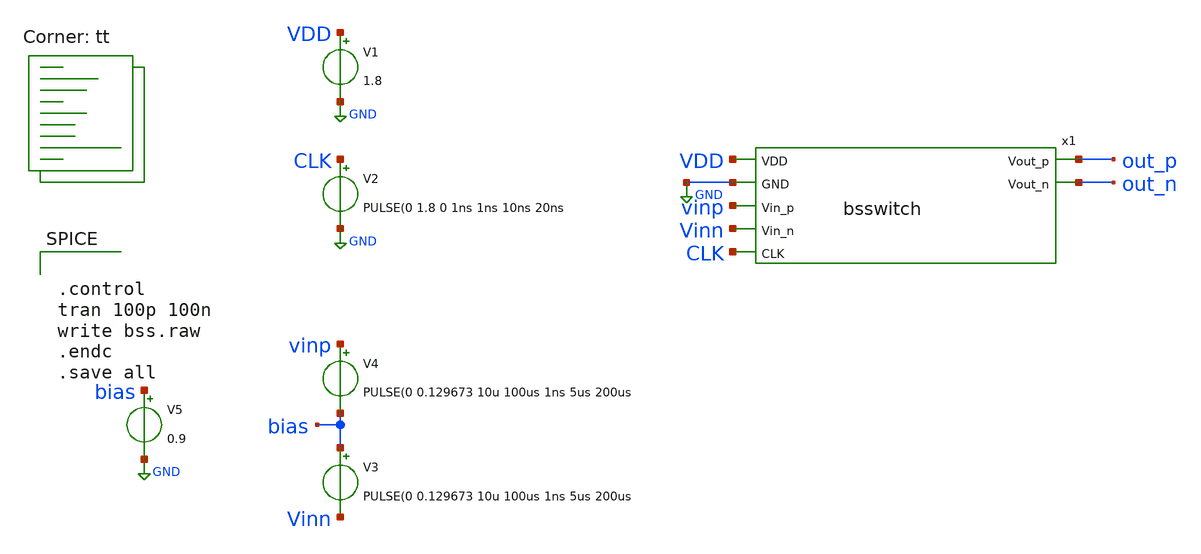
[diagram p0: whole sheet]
** sch_path: xschem/bsswitch_test.sch
**.subckt bsswitch_test
V2 CLK GND PULSE(0 1.8 0 1ns 1ns 10ns 20ns
V1 VDD GND 1.8
V3 bias Vinn PULSE(0 0.129673 10u 100us 1ns 5us 200us
V4 vinp bias PULSE(0 0.129673 10u 100us 1ns 5us 200us
V5 bias GND 0.9
x1 VDD GND vinp Vinn CLK out_p out_n bsswitch
**** begin user architecture code
.lib $::SKYWATER_MODELS/sky130.lib.spice tt


.control
tran 100p 100n
write bss.raw
.endc
.save all



*.lib $::SKYWATER_MODELS/sky130.lib.spice tt

* .lib $::SKYWATER_MODELS/sky130.lib.spice.tt.red tt

.include $::SKYWATER_STDCELLS/sky130_fd_sc_hd.spice

**** end user architecture code
**.ends

* expanding   symbol:  bsswitch.sym # of pins=7
** sym_path: xschem/bootstrapped_switch/bsswitch.sym
** sch_path: xschem/bootstrapped_switch/bsswitch.sch
.subckt bsswitch VDD GND Vin_p Vin_n CLK Vout_p Vout_n
*.ipin Vin_p
*.ipin Vin_n
*.ipin CLK
*.opin Vout_p
*.opin Vout_n
*.iopin VDD
*.iopin GND
XM11 net1 CLK VDD VDD sky130_fd_pr__pfet_01v8 L=0.15 W=1.605 nf=1 ad='int((nf+1)/2) * W/nf * 0.29' as='int((nf+2)/2) * W/nf * 0.29'
+ pd='2*int((nf+1)/2) * (W/nf + 0.29)' ps='2*int((nf+2)/2) * (W/nf + 0.29)' nrd='0.29 / W' nrs='0.29 / W'
+ sa=0 sb=0 sd=0 mult=1 m=1
XM12 net1 CLK net3 GND sky130_fd_pr__nfet_01v8 L=0.15 W=0.91 nf=1 ad='int((nf+1)/2) * W/nf * 0.29' as='int((nf+2)/2) * W/nf * 0.29'
+ pd='2*int((nf+1)/2) * (W/nf + 0.29)' ps='2*int((nf+2)/2) * (W/nf + 0.29)' nrd='0.29 / W' nrs='0.29 / W'
+ sa=0 sb=0 sd=0 mult=1 m=1
XM1 net2 net4 VDD net2 sky130_fd_pr__pfet_01v8 L=0.15 W=5 nf=1 ad='int((nf+1)/2) * W/nf * 0.29' as='int((nf+2)/2) * W/nf * 0.29'
+ pd='2*int((nf+1)/2) * (W/nf + 0.29)' ps='2*int((nf+2)/2) * (W/nf + 0.29)' nrd='0.29 / W' nrs='0.29 / W'
+ sa=0 sb=0 sd=0 mult=1 m=1
XM2 net4 net1 net2 net2 sky130_fd_pr__pfet_01v8 L=0.15 W=1.605 nf=1 ad='int((nf+1)/2) * W/nf * 0.29'
+ as='int((nf+2)/2) * W/nf * 0.29' pd='2*int((nf+1)/2) * (W/nf + 0.29)' ps='2*int((nf+2)/2) * (W/nf + 0.29)'
+ nrd='0.29 / W' nrs='0.29 / W' sa=0 sb=0 sd=0 mult=1 m=1
XM3 net4 VDD net5 GND sky130_fd_pr__nfet_01v8 L=0.15 W=0.91 nf=1 ad='int((nf+1)/2) * W/nf * 0.29' as='int((nf+2)/2) * W/nf * 0.29'
+ pd='2*int((nf+1)/2) * (W/nf + 0.29)' ps='2*int((nf+2)/2) * (W/nf + 0.29)' nrd='0.29 / W' nrs='0.29 / W'
+ sa=0 sb=0 sd=0 mult=2 m=2
XM4 net5 nCLK GND GND sky130_fd_pr__nfet_01v8 L=0.15 W=0.91 nf=1 ad='int((nf+1)/2) * W/nf * 0.29' as='int((nf+2)/2) * W/nf * 0.29'
+ pd='2*int((nf+1)/2) * (W/nf + 0.29)' ps='2*int((nf+2)/2) * (W/nf + 0.29)' nrd='0.29 / W' nrs='0.29 / W'
+ sa=0 sb=0 sd=0 mult=1 m=1
XM5 net3 net4 net1 GND sky130_fd_pr__nfet_01v8 L=0.15 W=0.91 nf=1 ad='int((nf+1)/2) * W/nf * 0.29' as='int((nf+2)/2) * W/nf * 0.29'
+ pd='2*int((nf+1)/2) * (W/nf + 0.29)' ps='2*int((nf+2)/2) * (W/nf + 0.29)' nrd='0.29 / W' nrs='0.29 / W'
+ sa=0 sb=0 sd=0 mult=1 m=1
XM6 Vin_p net4 net3 GND sky130_fd_pr__nfet_01v8 L=0.15 W=0.91 nf=1 ad='int((nf+1)/2) * W/nf * 0.29' as='int((nf+2)/2) * W/nf * 0.29'
+ pd='2*int((nf+1)/2) * (W/nf + 0.29)' ps='2*int((nf+2)/2) * (W/nf + 0.29)' nrd='0.29 / W' nrs='0.29 / W'
+ sa=0 sb=0 sd=0 mult=1 m=1
XM8 net3 nCLK GND GND sky130_fd_pr__nfet_01v8 L=0.15 W=0.91 nf=1 ad='int((nf+1)/2) * W/nf * 0.29' as='int((nf+2)/2) * W/nf * 0.29'
+ pd='2*int((nf+1)/2) * (W/nf + 0.29)' ps='2*int((nf+2)/2) * (W/nf + 0.29)' nrd='0.29 / W' nrs='0.29 / W'
+ sa=0 sb=0 sd=0 mult=8 m=8
XM9 net6 CLK VDD VDD sky130_fd_pr__pfet_01v8 L=0.15 W=1.605 nf=1 ad='int((nf+1)/2) * W/nf * 0.29' as='int((nf+2)/2) * W/nf * 0.29'
+ pd='2*int((nf+1)/2) * (W/nf + 0.29)' ps='2*int((nf+2)/2) * (W/nf + 0.29)' nrd='0.29 / W' nrs='0.29 / W'
+ sa=0 sb=0 sd=0 mult=1 m=1
XM10 net6 CLK net8 GND sky130_fd_pr__nfet_01v8 L=0.15 W=0.91 nf=1 ad='int((nf+1)/2) * W/nf * 0.29' as='int((nf+2)/2) * W/nf * 0.29'
+ pd='2*int((nf+1)/2) * (W/nf + 0.29)' ps='2*int((nf+2)/2) * (W/nf + 0.29)' nrd='0.29 / W' nrs='0.29 / W'
+ sa=0 sb=0 sd=0 mult=1 m=1
XM13 net7 net9 VDD net7 sky130_fd_pr__pfet_01v8 L=0.15 W=5 nf=1 ad='int((nf+1)/2) * W/nf * 0.29' as='int((nf+2)/2) * W/nf * 0.29'
+ pd='2*int((nf+1)/2) * (W/nf + 0.29)' ps='2*int((nf+2)/2) * (W/nf + 0.29)' nrd='0.29 / W' nrs='0.29 / W'
+ sa=0 sb=0 sd=0 mult=1 m=1
XM14 net9 net6 net7 net7 sky130_fd_pr__pfet_01v8 L=0.15 W=1.605 nf=1 ad='int((nf+1)/2) * W/nf * 0.29'
+ as='int((nf+2)/2) * W/nf * 0.29' pd='2*int((nf+1)/2) * (W/nf + 0.29)' ps='2*int((nf+2)/2) * (W/nf + 0.29)'
+ nrd='0.29 / W' nrs='0.29 / W' sa=0 sb=0 sd=0 mult=1 m=1
XM15 net9 VDD net10 GND sky130_fd_pr__nfet_01v8 L=0.15 W=0.91 nf=1 ad='int((nf+1)/2) * W/nf * 0.29' as='int((nf+2)/2) * W/nf * 0.29'
+ pd='2*int((nf+1)/2) * (W/nf + 0.29)' ps='2*int((nf+2)/2) * (W/nf + 0.29)' nrd='0.29 / W' nrs='0.29 / W'
+ sa=0 sb=0 sd=0 mult=2 m=2
XM16 net10 nCLK GND GND sky130_fd_pr__nfet_01v8 L=0.15 W=0.91 nf=1 ad='int((nf+1)/2) * W/nf * 0.29' as='int((nf+2)/2) * W/nf * 0.29'
+ pd='2*int((nf+1)/2) * (W/nf + 0.29)' ps='2*int((nf+2)/2) * (W/nf + 0.29)' nrd='0.29 / W' nrs='0.29 / W'
+ sa=0 sb=0 sd=0 mult=1 m=1
XM17 net8 net9 net6 GND sky130_fd_pr__nfet_01v8 L=0.15 W=0.91 nf=1 ad='int((nf+1)/2) * W/nf * 0.29' as='int((nf+2)/2) * W/nf * 0.29'
+ pd='2*int((nf+1)/2) * (W/nf + 0.29)' ps='2*int((nf+2)/2) * (W/nf + 0.29)' nrd='0.29 / W' nrs='0.29 / W'
+ sa=0 sb=0 sd=0 mult=1 m=1
XM18 Vin_n net9 net8 GND sky130_fd_pr__nfet_01v8 L=0.15 W=0.91 nf=1 ad='int((nf+1)/2) * W/nf * 0.29'
+ as='int((nf+2)/2) * W/nf * 0.29' pd='2*int((nf+1)/2) * (W/nf + 0.29)' ps='2*int((nf+2)/2) * (W/nf + 0.29)'
+ nrd='0.29 / W' nrs='0.29 / W' sa=0 sb=0 sd=0 mult=1 m=1
XM20 net8 nCLK GND GND sky130_fd_pr__nfet_01v8 L=0.15 W=0.91 nf=1 ad='int((nf+1)/2) * W/nf * 0.29' as='int((nf+2)/2) * W/nf * 0.29'
+ pd='2*int((nf+1)/2) * (W/nf + 0.29)' ps='2*int((nf+2)/2) * (W/nf + 0.29)' nrd='0.29 / W' nrs='0.29 / W'
+ sa=0 sb=0 sd=0 mult=8 m=8
XC3 net7 net8 sky130_fd_pr__cap_mim_m3_1 W=30 L=30 MF=1 m=1
XM19 Vin_n net9 Vout_n GND sky130_fd_pr__nfet_01v8 L=0.15 W=4.55 nf=1 ad='int((nf+1)/2) * W/nf * 0.29'
+ as='int((nf+2)/2) * W/nf * 0.29' pd='2*int((nf+1)/2) * (W/nf + 0.29)' ps='2*int((nf+2)/2) * (W/nf + 0.29)'
+ nrd='0.29 / W' nrs='0.29 / W' sa=0 sb=0 sd=0 mult=75 m=75
XM21 Vin_p net4 Vout_p GND sky130_fd_pr__nfet_01v8 L=0.15 W=4.55 nf=1 ad='int((nf+1)/2) * W/nf * 0.29'
+ as='int((nf+2)/2) * W/nf * 0.29' pd='2*int((nf+1)/2) * (W/nf + 0.29)' ps='2*int((nf+2)/2) * (W/nf + 0.29)'
+ nrd='0.29 / W' nrs='0.29 / W' sa=0 sb=0 sd=0 mult=75 m=75
XC1 net2 net3 sky130_fd_pr__cap_mim_m3_1 W=30 L=30 MF=1 m=1
x1 CLK GND GND VDD VDD nCLK sky130_fd_sc_hd__clkinv_1
.ends

.GLOBAL GND
.end
